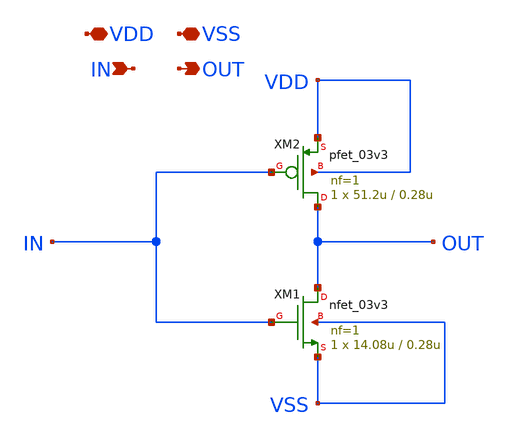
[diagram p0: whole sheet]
** sch_path: Clock_Generator_PAKISTAN_02/Schematics/INV_BUFF.sch
**.subckt INV_BUFF VDD VSS IN OUT
*.iopin VDD
*.iopin VSS
*.ipin IN
*.opin OUT
XM1 OUT IN VSS VSS nfet_03v3 L=0.28u W=14.08u nf=1 ad='int((nf+1)/2) * W/nf * 0.18u' as='int((nf+2)/2) * W/nf * 0.18u'
+ pd='2*int((nf+1)/2) * (W/nf + 0.18u)' ps='2*int((nf+2)/2) * (W/nf + 0.18u)' nrd='0.18u / W' nrs='0.18u / W'
+ sa=0 sb=0 sd=0 m=1
XM2 OUT IN VDD VDD pfet_03v3 L=0.28u W=51.2u nf=1 ad='int((nf+1)/2) * W/nf * 0.18u' as='int((nf+2)/2) * W/nf * 0.18u'
+ pd='2*int((nf+1)/2) * (W/nf + 0.18u)' ps='2*int((nf+2)/2) * (W/nf + 0.18u)' nrd='0.18u / W' nrs='0.18u / W'
+ sa=0 sb=0 sd=0 m=1
**.ends
.end
